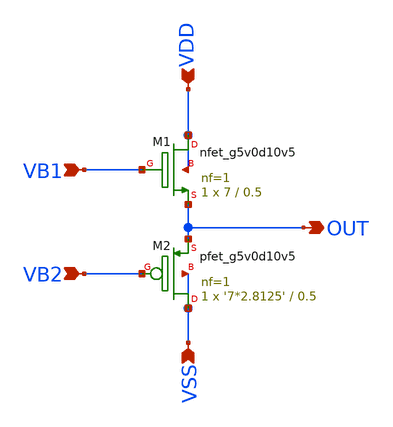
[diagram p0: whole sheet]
** sch_path: schem/voltage-reg.sch
**.subckt voltage-reg OUT VSS VB1 VDD VB2
*.opin OUT
*.ipin VSS
*.ipin VB1
*.ipin VDD
*.ipin VB2
XM1 VDD VB1 OUT VDD sky130_fd_pr__nfet_g5v0d10v5 L=0.5 W=7 nf=1 ad='int((nf+1)/2) * W/nf * 0.29' as='int((nf+2)/2) * W/nf * 0.29'
+ pd='2*int((nf+1)/2) * (W/nf + 0.29)' ps='2*int((nf+2)/2) * (W/nf + 0.29)' nrd='0.29 / W' nrs='0.29 / W'
+ sa=0 sb=0 sd=0 mult=1 m=1
XM2 VSS VB2 OUT VSS sky130_fd_pr__pfet_g5v0d10v5 L=0.5 W='7*2.8125' nf=1 ad='int((nf+1)/2) * W/nf * 0.29'
+ as='int((nf+2)/2) * W/nf * 0.29' pd='2*int((nf+1)/2) * (W/nf + 0.29)' ps='2*int((nf+2)/2) * (W/nf + 0.29)'
+ nrd='0.29 / W' nrs='0.29 / W' sa=0 sb=0 sd=0 mult=1 m=1
**.ends
.end
